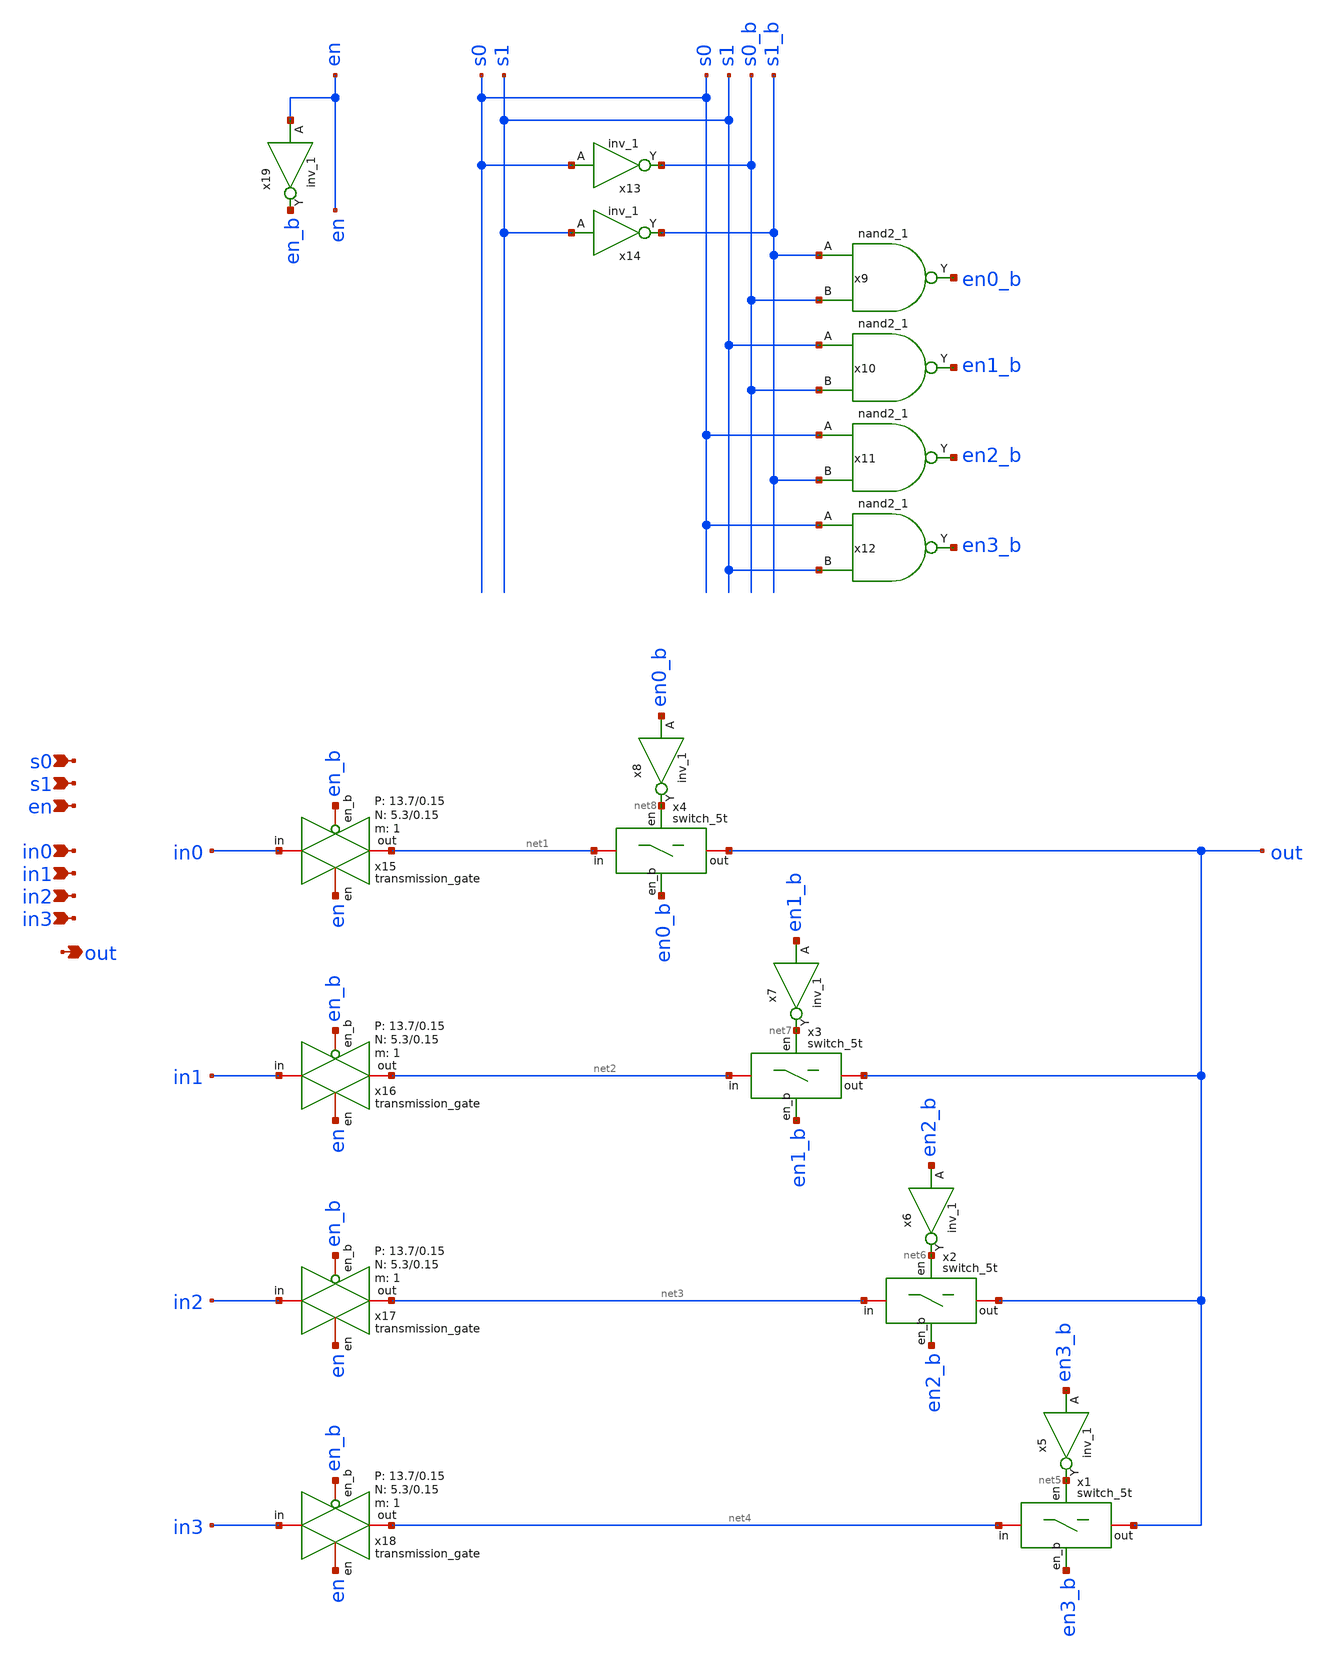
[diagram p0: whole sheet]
** sch_path: design/analog_modulator/schematic/a_mux4_en.sch
**.subckt a_mux4_en en s1 s0 in0 in1 in2 in3 out
*.ipin en
*.ipin s1
*.ipin s0
*.ipin in0
*.ipin in1
*.ipin in2
*.ipin in3
*.opin out
x1 net4 out net5 en3_b VDD VSS switch_5t
x2 net3 out net6 en2_b VDD VSS switch_5t
x3 net2 out net7 en1_b VDD VSS switch_5t
x4 net1 out net8 en0_b VDD VSS switch_5t
x5 en3_b VSS VSS VDD VDD net5 sky130_fd_sc_hd__inv_1
x6 en2_b VSS VSS VDD VDD net6 sky130_fd_sc_hd__inv_1
x7 en1_b VSS VSS VDD VDD net7 sky130_fd_sc_hd__inv_1
x8 en0_b VSS VSS VDD VDD net8 sky130_fd_sc_hd__inv_1
x13 s0 VSS VSS VDD VDD s0_b sky130_fd_sc_hd__inv_1
x14 s1 VSS VSS VDD VDD s1_b sky130_fd_sc_hd__inv_1
x9 s1_b s0_b VSS VSS VDD VDD en0_b sky130_fd_sc_hd__nand2_1
x10 s1 s0_b VSS VSS VDD VDD en1_b sky130_fd_sc_hd__nand2_1
x11 s0 s1_b VSS VSS VDD VDD en2_b sky130_fd_sc_hd__nand2_1
x12 s0 s1 VSS VSS VDD VDD en3_b sky130_fd_sc_hd__nand2_1
x15 in0 net1 en en_b VDD VSS 1 5.3 0.15 13.7 0.15 transmission_gate
x16 in1 net2 en en_b VDD VSS 1 5.3 0.15 13.7 0.15 transmission_gate
x17 in2 net3 en en_b VDD VSS 1 5.3 0.15 13.7 0.15 transmission_gate
x18 in3 net4 en en_b VDD VSS 1 5.3 0.15 13.7 0.15 transmission_gate
x19 en VSS VSS VDD VDD en_b sky130_fd_sc_hd__inv_1
**.ends

* expanding   symbol:  switch_5t.sym # of pins=4
** sym_path: design/analog_modulator/schematic/switch_5t.sym
** sch_path: design/analog_modulator/schematic/switch_5t.sch
.subckt switch_5t in out en en_b VDD VSS
*.iopin in
*.iopin out
*.ipin en
*.ipin en_b
x1 in net1 en en_b VDD VSS 1 5.3 0.15 13.7 0.15 transmission_gate
x2 net1 out en en_b VDD VSS 1 5.3 0.15 13.7 0.15 transmission_gate
XM1 net1 en_b VSS VSS sky130_fd_pr__nfet_01v8 L=0.15 W=0.5 nf=1 ad='int((nf+1)/2) * W/nf * 0.29' as='int((nf+2)/2) * W/nf * 0.29'
+ pd='2*int((nf+1)/2) * (W/nf + 0.29)' ps='2*int((nf+2)/2) * (W/nf + 0.29)' nrd='0.29 / W' nrs='0.29 / W'
+ sa=0 sb=0 sd=0 mult=1 m=1
.ends


* expanding   symbol:  transmission_gate.sym # of pins=4
** sym_path: design/analog_modulator/schematic/transmission_gate.sym
** sch_path: design/analog_modulator/schematic/transmission_gate.sch
.subckt transmission_gate in out en en_b VDD VSS N W_N L_N W_P L_P    N=1 W_N=5.3 L_N=0.15 W_P=13.7
+ L_P=0.15
*.iopin in
*.iopin out
*.ipin en
*.ipin en_b
XM1 out en in VSS sky130_fd_pr__nfet_01v8 L='L_N' W='W_N' nf=1 ad='int((nf+1)/2) * W/nf * 0.29' as='int((nf+2)/2) * W/nf * 0.29'
+ pd='2*int((nf+1)/2) * (W/nf + 0.29)' ps='2*int((nf+2)/2) * (W/nf + 0.29)' nrd='0.29 / W' nrs='0.29 / W'
+ sa=0 sb=0 sd=0 mult='N' m='N'
XM2 out en_b in VDD sky130_fd_pr__pfet_01v8 L='L_P' W='W_P' nf=1 ad='int((nf+1)/2) * W/nf * 0.29' as='int((nf+2)/2) * W/nf * 0.29'
+ pd='2*int((nf+1)/2) * (W/nf + 0.29)' ps='2*int((nf+2)/2) * (W/nf + 0.29)' nrd='0.29 / W' nrs='0.29 / W'
+ sa=0 sb=0 sd=0 mult='N' m='N'
.ends

.end
